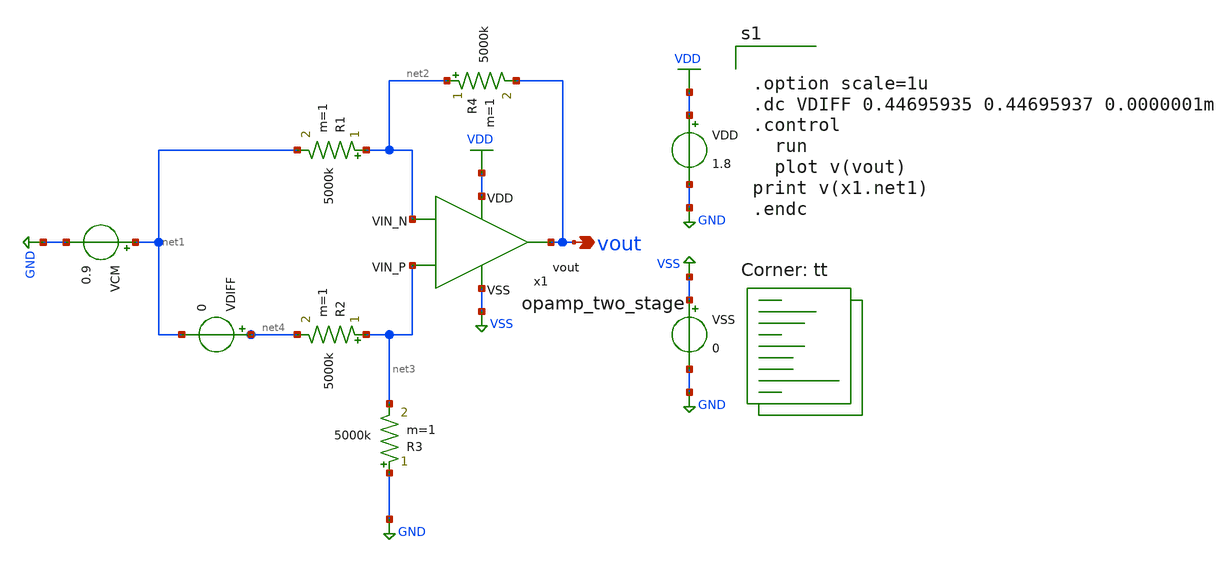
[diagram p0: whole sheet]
** sch_path: analog/schematics/tb_dc_analysis.sch
**.subckt tb_dc_analysis vout
*.opin vout
VDD VDD GND 1.8
VSS VSS GND 0
VCM net1 GND 0.9
VDIFF net4 net1 0
R1 net2 net1 5000k m=1
R2 net3 net4 5000k m=1
R3 GND net3 5000k m=1
R4 net2 vout 5000k m=1
x1 VDD vout net3 net2 VSS opamp_two_stage
**** begin user architecture code


.option scale=1u
.dc VDIFF 0.44695935 0.44695937 0.0000001m
.control
  run
  plot v(vout)
print v(x1.net1)
.endc


.lib $::SKYWATER_MODELS/sky130.lib.spice tt
**** end user architecture code
**.ends

* expanding   symbol:  opamp_two_stage.sym # of pins=5
** sym_path: analog/schematics/opamp_two_stage.sym
** sch_path: analog/schematics/opamp_two_stage.sch
.subckt opamp_two_stage VDD vout VIN_P VIN_N VSS
*.ipin VIN_P
*.ipin VIN_N
*.opin vout
*.ipin VDD
*.ipin VSS
XM1 net3 VIN_N net4 VSS sky130_fd_pr__nfet_01v8 L=8 W=7 nf=1 ad='int((nf+1)/2) * W/nf * 0.29' as='int((nf+2)/2) * W/nf * 0.29'
+ pd='2*int((nf+1)/2) * (W/nf + 0.29)' ps='2*int((nf+2)/2) * (W/nf + 0.29)' nrd='0.29 / W' nrs='0.29 / W'
+ sa=0 sb=0 sd=0 mult=1 m=1
XM2 net5 VIN_P net4 VSS sky130_fd_pr__nfet_01v8 L=8 W=7 nf=1 ad='int((nf+1)/2) * W/nf * 0.29' as='int((nf+2)/2) * W/nf * 0.29'
+ pd='2*int((nf+1)/2) * (W/nf + 0.29)' ps='2*int((nf+2)/2) * (W/nf + 0.29)' nrd='0.29 / W' nrs='0.29 / W'
+ sa=0 sb=0 sd=0 mult=1 m=1
XM3 net3 net5 VDD VDD sky130_fd_pr__pfet_01v8 L=8 W=7 nf=1 ad='int((nf+1)/2) * W/nf * 0.29' as='int((nf+2)/2) * W/nf * 0.29'
+ pd='2*int((nf+1)/2) * (W/nf + 0.29)' ps='2*int((nf+2)/2) * (W/nf + 0.29)' nrd='0.29 / W' nrs='0.29 / W'
+ sa=0 sb=0 sd=0 mult=1 m=1
XM4 net5 net5 VDD VDD sky130_fd_pr__pfet_01v8 L=8 W=7 nf=1 ad='int((nf+1)/2) * W/nf * 0.29' as='int((nf+2)/2) * W/nf * 0.29'
+ pd='2*int((nf+1)/2) * (W/nf + 0.29)' ps='2*int((nf+2)/2) * (W/nf + 0.29)' nrd='0.29 / W' nrs='0.29 / W'
+ sa=0 sb=0 sd=0 mult=1 m=1
XM5 vout net3 VDD VDD sky130_fd_pr__pfet_01v8 L=8 W=7 nf=1 ad='int((nf+1)/2) * W/nf * 0.29' as='int((nf+2)/2) * W/nf * 0.29'
+ pd='2*int((nf+1)/2) * (W/nf + 0.29)' ps='2*int((nf+2)/2) * (W/nf + 0.29)' nrd='0.29 / W' nrs='0.29 / W'
+ sa=0 sb=0 sd=0 mult=2 m=2
XM6 vout net1 VSS VSS sky130_fd_pr__nfet_01v8 L=8 W=7 nf=1 ad='int((nf+1)/2) * W/nf * 0.29' as='int((nf+2)/2) * W/nf * 0.29'
+ pd='2*int((nf+1)/2) * (W/nf + 0.29)' ps='2*int((nf+2)/2) * (W/nf + 0.29)' nrd='0.29 / W' nrs='0.29 / W'
+ sa=0 sb=0 sd=0 mult=2 m=2
XM7 net4 net1 VSS VSS sky130_fd_pr__nfet_01v8 L=8 W=7 nf=1 ad='int((nf+1)/2) * W/nf * 0.29' as='int((nf+2)/2) * W/nf * 0.29'
+ pd='2*int((nf+1)/2) * (W/nf + 0.29)' ps='2*int((nf+2)/2) * (W/nf + 0.29)' nrd='0.29 / W' nrs='0.29 / W'
+ sa=0 sb=0 sd=0 mult=2 m=2
XR1 net3 net2 VSS sky130_fd_pr__res_high_po W=1 L=1 mult=1 m=1
XC1 vout net2 sky130_fd_pr__cap_mim_m3_1 W=1 L=1 MF=1 m=1
XR2 net1 VDD VSS sky130_fd_pr__res_high_po W=1 L=1 mult=1 m=1
XR3 VSS net1 VSS sky130_fd_pr__res_high_po W=1 L=1 mult=1 m=1
.ends

.GLOBAL VDD
.GLOBAL GND
.GLOBAL VSS
.end
